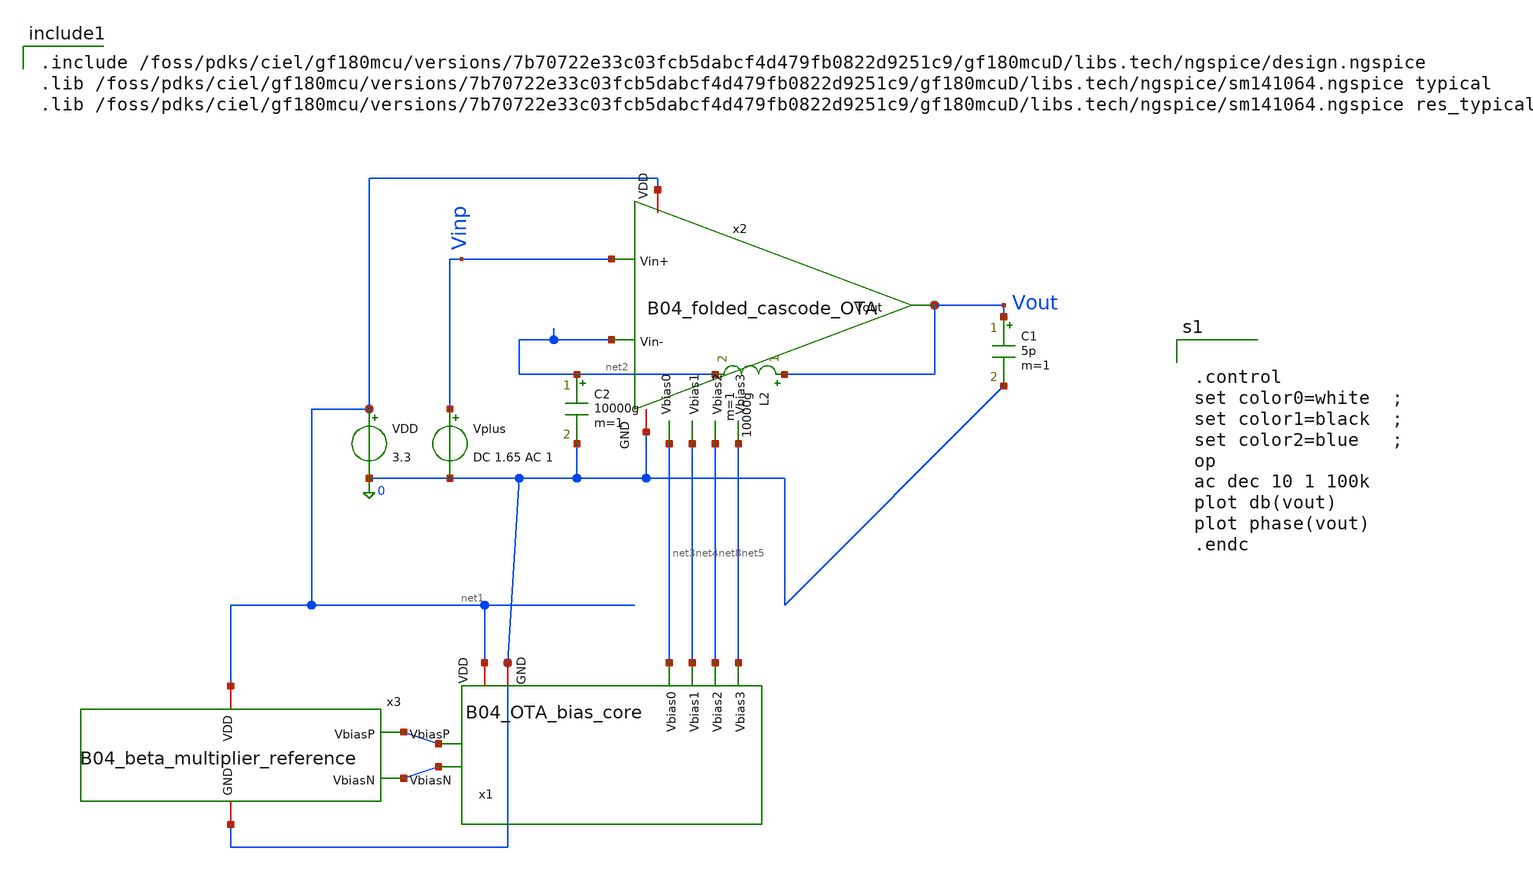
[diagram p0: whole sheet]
** sch_path: analog/B04_tb_OTA.sch
**.subckt B04_tb_OTA
VDD net1 0 3.3
Vplus Vinp 0 DC 1.65 AC 1
x1 net1 net6 net3 net8 net5 net4 net7 0 B04_OTA_bias_core ratio=0.25
x3 net1 net6 net7 0 B04_beta_multiplier_reference length=410u
C1 Vout 0 5p m=1
C2 net2 0 10000g m=1
L2 Vout net2 10000g m=1
x2 net1 net3 Vinp net2 net5 net4 Vout net8 0 B04_folded_cascode_OTA
**** begin user architecture code


.control
set color0=white  ;
set color1=black  ;
set color2=blue   ;
op
ac dec 10 1 100k
plot db(vout)
plot phase(vout)
.endc



.include /foss/pdks/ciel/gf180mcu/versions/7b70722e33c03fcb5dabcf4d479fb0822d9251c9/gf180mcuD/libs.tech/ngspice/design.ngspice
.lib /foss/pdks/ciel/gf180mcu/versions/7b70722e33c03fcb5dabcf4d479fb0822d9251c9/gf180mcuD/libs.tech/ngspice/sm141064.ngspice typical
.lib /foss/pdks/ciel/gf180mcu/versions/7b70722e33c03fcb5dabcf4d479fb0822d9251c9/gf180mcuD/libs.tech/ngspice/sm141064.ngspice res_typical

**** end user architecture code
**.ends

* expanding   symbol:
*+  AURA-Event-Driven-Mixed-Signal-ASIC-for-Acoustic-Pattern-Detection/analog/B04_OTA_bias_core.sym # of pins=8
** sym_path: analog/B04_OTA_bias_core.sym
** sch_path: analog/B04_OTA_bias_core.sch
.subckt B04_OTA_bias_core VDD VbiasP Vbias0 Vbias2 Vbias3 Vbias1 VbiasN GND  ratio=1
*.iopin VDD
*.opin Vbias2
*.opin Vbias1
*.opin Vbias0
*.opin Vbias3
*.iopin GND
*.ipin VbiasP
*.ipin VbiasN
XM1 Vbias1 GND Vbias2 VDD pfet_03v3 L=4u W=5u nf=1 ad='int((nf+1)/2) * W/nf * 0.18u' as='int((nf+2)/2) * W/nf * 0.18u'
+ pd='2*int((nf+1)/2) * (W/nf + 0.18u)' ps='2*int((nf+2)/2) * (W/nf + 0.18u)' nrd='0.18u / W' nrs='0.18u / W'
+ sa=0 sb=0 sd=0 m=1
XM4 Vbias1 Vbias2 net1 GND nfet_03v3 L=4u W=1u nf=1 ad='int((nf+1)/2) * W/nf * 0.18u' as='int((nf+2)/2) * W/nf * 0.18u'
+ pd='2*int((nf+1)/2) * (W/nf + 0.18u)' ps='2*int((nf+2)/2) * (W/nf + 0.18u)' nrd='0.18u / W' nrs='0.18u / W'
+ sa=0 sb=0 sd=0 m=1
XM5 net1 Vbias1 GND GND nfet_03v3 L=4u W=1u nf=1 ad='int((nf+1)/2) * W/nf * 0.18u' as='int((nf+2)/2) * W/nf * 0.18u'
+ pd='2*int((nf+1)/2) * (W/nf + 0.18u)' ps='2*int((nf+2)/2) * (W/nf + 0.18u)' nrd='0.18u / W' nrs='0.18u / W'
+ sa=0 sb=0 sd=0 m=1
XM9 net2 Vbias3 Vbias0 VDD pfet_03v3 L=4u W=5u nf=1 ad='int((nf+1)/2) * W/nf * 0.18u' as='int((nf+2)/2) * W/nf * 0.18u'
+ pd='2*int((nf+1)/2) * (W/nf + 0.18u)' ps='2*int((nf+2)/2) * (W/nf + 0.18u)' nrd='0.18u / W' nrs='0.18u / W'
+ sa=0 sb=0 sd=0 m=1
XM10 VDD Vbias0 net2 VDD pfet_03v3 L=4u W=5u nf=1 ad='int((nf+1)/2) * W/nf * 0.18u' as='int((nf+2)/2) * W/nf * 0.18u'
+ pd='2*int((nf+1)/2) * (W/nf + 0.18u)' ps='2*int((nf+2)/2) * (W/nf + 0.18u)' nrd='0.18u / W' nrs='0.18u / W'
+ sa=0 sb=0 sd=0 m=1
XM6 Vbias3 VDD Vbias0 GND nfet_03v3 L=4u W=10u nf=1 ad='int((nf+1)/2) * W/nf * 0.18u' as='int((nf+2)/2) * W/nf * 0.18u'
+ pd='2*int((nf+1)/2) * (W/nf + 0.18u)' ps='2*int((nf+2)/2) * (W/nf + 0.18u)' nrd='0.18u / W' nrs='0.18u / W'
+ sa=0 sb=0 sd=0 m=1
XM2 Vbias2 VbiasP VDD VDD pfet_03v3 L=4u W={ratio*5u} nf=1 ad='int((nf+1)/2) * W/nf * 0.18u' as='int((nf+2)/2) * W/nf * 0.18u'
+ pd='2*int((nf+1)/2) * (W/nf + 0.18u)' ps='2*int((nf+2)/2) * (W/nf + 0.18u)' nrd='0.18u / W' nrs='0.18u / W'
+ sa=0 sb=0 sd=0 m=1
XM3 GND VbiasN Vbias3 GND nfet_03v3 L=4u W={ratio*10u} nf=1 ad='int((nf+1)/2) * W/nf * 0.18u' as='int((nf+2)/2) * W/nf * 0.18u'
+ pd='2*int((nf+1)/2) * (W/nf + 0.18u)' ps='2*int((nf+2)/2) * (W/nf + 0.18u)' nrd='0.18u / W' nrs='0.18u / W'
+ sa=0 sb=0 sd=0 m=1
.ends


* expanding   symbol:
*+  AURA-Event-Driven-Mixed-Signal-ASIC-for-Acoustic-Pattern-Detection/analog/B04_beta_multiplier_reference.sym # of pins=4
** sym_path: analog/B04_beta_multiplier_reference.sym
** sch_path: analog/B04_beta_multiplier_reference.sch
.subckt B04_beta_multiplier_reference VDD VbiasP VbiasN GND  length=410u
*.iopin VDD
*.iopin GND
*.opin VbiasP
*.opin VbiasN
XM2 VbiasN VbiasP VDD VDD pfet_03v3 L=4u W=2u nf=1 ad='int((nf+1)/2) * W/nf * 0.18u' as='int((nf+2)/2) * W/nf * 0.18u'
+ pd='2*int((nf+1)/2) * (W/nf + 0.18u)' ps='2*int((nf+2)/2) * (W/nf + 0.18u)' nrd='0.18u / W' nrs='0.18u / W'
+ sa=0 sb=0 sd=0 m=1
XM3 net2 VbiasP VDD VDD pfet_03v3 L=4u W=2u nf=1 ad='int((nf+1)/2) * W/nf * 0.18u' as='int((nf+2)/2) * W/nf * 0.18u'
+ pd='2*int((nf+1)/2) * (W/nf + 0.18u)' ps='2*int((nf+2)/2) * (W/nf + 0.18u)' nrd='0.18u / W' nrs='0.18u / W'
+ sa=0 sb=0 sd=0 m=1
XM6 VbiasN VbiasN GND GND nfet_03v3 L=4u W=10u nf=1 ad='int((nf+1)/2) * W/nf * 0.18u' as='int((nf+2)/2) * W/nf * 0.18u'
+ pd='2*int((nf+1)/2) * (W/nf + 0.18u)' ps='2*int((nf+2)/2) * (W/nf + 0.18u)' nrd='0.18u / W' nrs='0.18u / W'
+ sa=0 sb=0 sd=0 m=1
XM7 net2 VbiasN net1 GND nfet_03v3 L=4u W=10u nf=1 ad='int((nf+1)/2) * W/nf * 0.18u' as='int((nf+2)/2) * W/nf * 0.18u'
+ pd='2*int((nf+1)/2) * (W/nf + 0.18u)' ps='2*int((nf+2)/2) * (W/nf + 0.18u)' nrd='0.18u / W' nrs='0.18u / W'
+ sa=0 sb=0 sd=0 m=4
XM1 net4 net4 VDD VDD pfet_03v3 L=40u W=0.22u nf=1 ad='int((nf+1)/2) * W/nf * 0.18u' as='int((nf+2)/2) * W/nf * 0.18u'
+ pd='2*int((nf+1)/2) * (W/nf + 0.18u)' ps='2*int((nf+2)/2) * (W/nf + 0.18u)' nrd='0.18u / W' nrs='0.18u / W'
+ sa=0 sb=0 sd=0 m=1
XM4 VbiasP net3 VbiasN GND nfet_03v3 L=1u W=1u nf=1 ad='int((nf+1)/2) * W/nf * 0.18u' as='int((nf+2)/2) * W/nf * 0.18u'
+ pd='2*int((nf+1)/2) * (W/nf + 0.18u)' ps='2*int((nf+2)/2) * (W/nf + 0.18u)' nrd='0.18u / W' nrs='0.18u / W'
+ sa=0 sb=0 sd=0 m=1
XM5 net3 VbiasN GND GND nfet_03v3 L=10u W=1u nf=1 ad='int((nf+1)/2) * W/nf * 0.18u' as='int((nf+2)/2) * W/nf * 0.18u'
+ pd='2*int((nf+1)/2) * (W/nf + 0.18u)' ps='2*int((nf+2)/2) * (W/nf + 0.18u)' nrd='0.18u / W' nrs='0.18u / W'
+ sa=0 sb=0 sd=0 m=1
XM8 net5 net5 net4 VDD pfet_03v3 L=40u W=0.22u nf=1 ad='int((nf+1)/2) * W/nf * 0.18u' as='int((nf+2)/2) * W/nf * 0.18u'
+ pd='2*int((nf+1)/2) * (W/nf + 0.18u)' ps='2*int((nf+2)/2) * (W/nf + 0.18u)' nrd='0.18u / W' nrs='0.18u / W'
+ sa=0 sb=0 sd=0 m=1
XM9 net3 net5 net5 VDD pfet_03v3 L=40u W=0.22u nf=1 ad='int((nf+1)/2) * W/nf * 0.18u' as='int((nf+2)/2) * W/nf * 0.18u'
+ pd='2*int((nf+1)/2) * (W/nf + 0.18u)' ps='2*int((nf+2)/2) * (W/nf + 0.18u)' nrd='0.18u / W' nrs='0.18u / W'
+ sa=0 sb=0 sd=0 m=1
XR2 GND net1 GND ppolyf_u_2k r_width=2u r_length={length} m=1
x1 VDD VbiasP net2 VbiasN VbiasN GND B04_diff_amp
.ends


* expanding   symbol:
*+  AURA-Event-Driven-Mixed-Signal-ASIC-for-Acoustic-Pattern-Detection/analog/B04_folded_cascode_OTA.sym # of pins=9
** sym_path: analog/B04_folded_cascode_OTA.sym
** sch_path: analog/B04_folded_cascode_OTA.sch
.subckt B04_folded_cascode_OTA VDD Vbias0 Vin+ Vin- Vbias3 Vbias1 Vout Vbias2 GND
*.iopin VDD
*.ipin Vbias0
*.ipin Vin+
*.ipin Vin-
*.opin Vout
*.ipin Vbias3
*.ipin Vbias2
*.iopin GND
*.ipin Vbias1
XM1 net1 Vbias0 VDD VDD pfet_03v3 L=4u W=5u nf=2 ad='int((nf+1)/2) * W/nf * 0.18u' as='int((nf+2)/2) * W/nf * 0.18u'
+ pd='2*int((nf+1)/2) * (W/nf + 0.18u)' ps='2*int((nf+2)/2) * (W/nf + 0.18u)' nrd='0.18u / W' nrs='0.18u / W'
+ sa=0 sb=0 sd=0 m=1
XM2 net6 Vin+ net1 VDD pfet_03v3 L=1u W=2u nf=9 ad='int((nf+1)/2) * W/nf * 0.18u' as='int((nf+2)/2) * W/nf * 0.18u'
+ pd='2*int((nf+1)/2) * (W/nf + 0.18u)' ps='2*int((nf+2)/2) * (W/nf + 0.18u)' nrd='0.18u / W' nrs='0.18u / W'
+ sa=0 sb=0 sd=0 m=1
XM3 net7 Vin- net1 VDD pfet_03v3 L=1u W=2u nf=9 ad='int((nf+1)/2) * W/nf * 0.18u' as='int((nf+2)/2) * W/nf * 0.18u'
+ pd='2*int((nf+1)/2) * (W/nf + 0.18u)' ps='2*int((nf+2)/2) * (W/nf + 0.18u)' nrd='0.18u / W' nrs='0.18u / W'
+ sa=0 sb=0 sd=0 m=1
XM4 net2 Vin+ net1 VDD pfet_03v3 L=1u W=2u nf=1 ad='int((nf+1)/2) * W/nf * 0.18u' as='int((nf+2)/2) * W/nf * 0.18u'
+ pd='2*int((nf+1)/2) * (W/nf + 0.18u)' ps='2*int((nf+2)/2) * (W/nf + 0.18u)' nrd='0.18u / W' nrs='0.18u / W'
+ sa=0 sb=0 sd=0 m=1
XM5 net3 Vin- net1 VDD pfet_03v3 L=1u W=2u nf=1 ad='int((nf+1)/2) * W/nf * 0.18u' as='int((nf+2)/2) * W/nf * 0.18u'
+ pd='2*int((nf+1)/2) * (W/nf + 0.18u)' ps='2*int((nf+2)/2) * (W/nf + 0.18u)' nrd='0.18u / W' nrs='0.18u / W'
+ sa=0 sb=0 sd=0 m=1
XM6 net2 Vbias2 net5 0 nfet_03v3 L=1u W=2u nf=1 ad='int((nf+1)/2) * W/nf * 0.18u' as='int((nf+2)/2) * W/nf * 0.18u'
+ pd='2*int((nf+1)/2) * (W/nf + 0.18u)' ps='2*int((nf+2)/2) * (W/nf + 0.18u)' nrd='0.18u / W' nrs='0.18u / W'
+ sa=0 sb=0 sd=0 m=1
XM7 net3 Vbias2 net4 0 nfet_03v3 L=1u W=2u nf=1 ad='int((nf+1)/2) * W/nf * 0.18u' as='int((nf+2)/2) * W/nf * 0.18u'
+ pd='2*int((nf+1)/2) * (W/nf + 0.18u)' ps='2*int((nf+2)/2) * (W/nf + 0.18u)' nrd='0.18u / W' nrs='0.18u / W'
+ sa=0 sb=0 sd=0 m=1
XM8 net5 net2 GND GND nfet_03v3 L=4u W=1u nf=1 ad='int((nf+1)/2) * W/nf * 0.18u' as='int((nf+2)/2) * W/nf * 0.18u'
+ pd='2*int((nf+1)/2) * (W/nf + 0.18u)' ps='2*int((nf+2)/2) * (W/nf + 0.18u)' nrd='0.18u / W' nrs='0.18u / W'
+ sa=0 sb=0 sd=0 m=1
XM9 net6 net3 GND GND nfet_03v3 L=4u W=1u nf=1 ad='int((nf+1)/2) * W/nf * 0.18u' as='int((nf+2)/2) * W/nf * 0.18u'
+ pd='2*int((nf+1)/2) * (W/nf + 0.18u)' ps='2*int((nf+2)/2) * (W/nf + 0.18u)' nrd='0.18u / W' nrs='0.18u / W'
+ sa=0 sb=0 sd=0 m=1
XM10 net4 net3 GND GND nfet_03v3 L=4u W=1u nf=1 ad='int((nf+1)/2) * W/nf * 0.18u' as='int((nf+2)/2) * W/nf * 0.18u'
+ pd='2*int((nf+1)/2) * (W/nf + 0.18u)' ps='2*int((nf+2)/2) * (W/nf + 0.18u)' nrd='0.18u / W' nrs='0.18u / W'
+ sa=0 sb=0 sd=0 m=1
XM11 net7 net2 GND GND nfet_03v3 L=4u W=1u nf=1 ad='int((nf+1)/2) * W/nf * 0.18u' as='int((nf+2)/2) * W/nf * 0.18u'
+ pd='2*int((nf+1)/2) * (W/nf + 0.18u)' ps='2*int((nf+2)/2) * (W/nf + 0.18u)' nrd='0.18u / W' nrs='0.18u / W'
+ sa=0 sb=0 sd=0 m=1
XM12 net9 net10 VDD VDD pfet_03v3 L=4u W=5u nf=1 ad='int((nf+1)/2) * W/nf * 0.18u' as='int((nf+2)/2) * W/nf * 0.18u'
+ pd='2*int((nf+1)/2) * (W/nf + 0.18u)' ps='2*int((nf+2)/2) * (W/nf + 0.18u)' nrd='0.18u / W' nrs='0.18u / W'
+ sa=0 sb=0 sd=0 m=1
XM13 net8 net10 VDD VDD pfet_03v3 L=4u W=5u nf=1 ad='int((nf+1)/2) * W/nf * 0.18u' as='int((nf+2)/2) * W/nf * 0.18u'
+ pd='2*int((nf+1)/2) * (W/nf + 0.18u)' ps='2*int((nf+2)/2) * (W/nf + 0.18u)' nrd='0.18u / W' nrs='0.18u / W'
+ sa=0 sb=0 sd=0 m=1
XM14 Vout Vbias3 net9 VDD pfet_03v3 L=4u W=5u nf=1 ad='int((nf+1)/2) * W/nf * 0.18u' as='int((nf+2)/2) * W/nf * 0.18u'
+ pd='2*int((nf+1)/2) * (W/nf + 0.18u)' ps='2*int((nf+2)/2) * (W/nf + 0.18u)' nrd='0.18u / W' nrs='0.18u / W'
+ sa=0 sb=0 sd=0 m=1
XM15 net10 Vbias3 net8 VDD pfet_03v3 L=4u W=5u nf=1 ad='int((nf+1)/2) * W/nf * 0.18u' as='int((nf+2)/2) * W/nf * 0.18u'
+ pd='2*int((nf+1)/2) * (W/nf + 0.18u)' ps='2*int((nf+2)/2) * (W/nf + 0.18u)' nrd='0.18u / W' nrs='0.18u / W'
+ sa=0 sb=0 sd=0 m=1
XM16 Vout Vbias2 net7 0 nfet_03v3 L=4u W=1u nf=1 ad='int((nf+1)/2) * W/nf * 0.18u' as='int((nf+2)/2) * W/nf * 0.18u'
+ pd='2*int((nf+1)/2) * (W/nf + 0.18u)' ps='2*int((nf+2)/2) * (W/nf + 0.18u)' nrd='0.18u / W' nrs='0.18u / W'
+ sa=0 sb=0 sd=0 m=1
XM17 net10 Vbias2 net6 0 nfet_03v3 L=4u W=1u nf=1 ad='int((nf+1)/2) * W/nf * 0.18u' as='int((nf+2)/2) * W/nf * 0.18u'
+ pd='2*int((nf+1)/2) * (W/nf + 0.18u)' ps='2*int((nf+2)/2) * (W/nf + 0.18u)' nrd='0.18u / W' nrs='0.18u / W'
+ sa=0 sb=0 sd=0 m=1
XM18 net6 Vbias1 GND GND nfet_03v3 L=4u W=1u nf=10 ad='int((nf+1)/2) * W/nf * 0.18u' as='int((nf+2)/2) * W/nf * 0.18u'
+ pd='2*int((nf+1)/2) * (W/nf + 0.18u)' ps='2*int((nf+2)/2) * (W/nf + 0.18u)' nrd='0.18u / W' nrs='0.18u / W'
+ sa=0 sb=0 sd=0 m=1
XM19 net7 Vbias1 GND GND nfet_03v3 L=4u W=1u nf=10 ad='int((nf+1)/2) * W/nf * 0.18u' as='int((nf+2)/2) * W/nf * 0.18u'
+ pd='2*int((nf+1)/2) * (W/nf + 0.18u)' ps='2*int((nf+2)/2) * (W/nf + 0.18u)' nrd='0.18u / W' nrs='0.18u / W'
+ sa=0 sb=0 sd=0 m=1
.ends


* expanding   symbol:
*+  AURA-Event-Driven-Mixed-Signal-ASIC-for-Acoustic-Pattern-Detection/analog/B04_diff_amp.sym # of pins=6
** sym_path: analog/B04_diff_amp.sym
** sch_path: analog/B04_diff_amp.sch
.subckt B04_diff_amp VDD Vo V+ V- Vbias VSS
*.iopin VDD
*.iopin VSS
*.ipin V+
*.ipin V-
*.opin Vo
*.ipin Vbias
XM1 net1 V+ net2 VSS nfet_03v3 L=4u W=1.1u nf=1 ad='int((nf+1)/2) * W/nf * 0.18u' as='int((nf+2)/2) * W/nf * 0.18u'
+ pd='2*int((nf+1)/2) * (W/nf + 0.18u)' ps='2*int((nf+2)/2) * (W/nf + 0.18u)' nrd='0.18u / W' nrs='0.18u / W'
+ sa=0 sb=0 sd=0 m=1
XM2 net2 Vbias VSS VSS nfet_03v3 L=4u W=2.2u nf=1 ad='int((nf+1)/2) * W/nf * 0.18u' as='int((nf+2)/2) * W/nf * 0.18u'
+ pd='2*int((nf+1)/2) * (W/nf + 0.18u)' ps='2*int((nf+2)/2) * (W/nf + 0.18u)' nrd='0.18u / W' nrs='0.18u / W'
+ sa=0 sb=0 sd=0 m=1
XM3 Vo V- net2 VSS nfet_03v3 L=4u W=1.1u nf=1 ad='int((nf+1)/2) * W/nf * 0.18u' as='int((nf+2)/2) * W/nf * 0.18u'
+ pd='2*int((nf+1)/2) * (W/nf + 0.18u)' ps='2*int((nf+2)/2) * (W/nf + 0.18u)' nrd='0.18u / W' nrs='0.18u / W'
+ sa=0 sb=0 sd=0 m=1
XM4 Vo net1 VDD VDD pfet_03v3 L=4u W=13u nf=1 ad='int((nf+1)/2) * W/nf * 0.18u' as='int((nf+2)/2) * W/nf * 0.18u'
+ pd='2*int((nf+1)/2) * (W/nf + 0.18u)' ps='2*int((nf+2)/2) * (W/nf + 0.18u)' nrd='0.18u / W' nrs='0.18u / W'
+ sa=0 sb=0 sd=0 m=1
XM5 net1 net1 VDD VDD pfet_03v3 L=4u W=13u nf=1 ad='int((nf+1)/2) * W/nf * 0.18u' as='int((nf+2)/2) * W/nf * 0.18u'
+ pd='2*int((nf+1)/2) * (W/nf + 0.18u)' ps='2*int((nf+2)/2) * (W/nf + 0.18u)' nrd='0.18u / W' nrs='0.18u / W'
+ sa=0 sb=0 sd=0 m=1
XMDummy VDD VDD VDD VDD pfet_03v3 L=4u W=6.5u nf=1 ad='int((nf+1)/2) * W/nf * 0.18u' as='int((nf+2)/2) * W/nf * 0.18u'
+ pd='2*int((nf+1)/2) * (W/nf + 0.18u)' ps='2*int((nf+2)/2) * (W/nf + 0.18u)' nrd='0.18u / W' nrs='0.18u / W'
+ sa=0 sb=0 sd=0 m=1
XMDummy1 VDD VDD VDD VDD pfet_03v3 L=4u W=6.5u nf=1 ad='int((nf+1)/2) * W/nf * 0.18u' as='int((nf+2)/2) * W/nf * 0.18u'
+ pd='2*int((nf+1)/2) * (W/nf + 0.18u)' ps='2*int((nf+2)/2) * (W/nf + 0.18u)' nrd='0.18u / W' nrs='0.18u / W'
+ sa=0 sb=0 sd=0 m=1
XMdummy2 VSS VSS VSS VSS nfet_03v3 L=4u W=0.55u nf=1 ad='int((nf+1)/2) * W/nf * 0.18u' as='int((nf+2)/2) * W/nf * 0.18u'
+ pd='2*int((nf+1)/2) * (W/nf + 0.18u)' ps='2*int((nf+2)/2) * (W/nf + 0.18u)' nrd='0.18u / W' nrs='0.18u / W'
+ sa=0 sb=0 sd=0 m=1
XMdummy3 VSS VSS VSS VSS nfet_03v3 L=4u W=0.55u nf=1 ad='int((nf+1)/2) * W/nf * 0.18u' as='int((nf+2)/2) * W/nf * 0.18u'
+ pd='2*int((nf+1)/2) * (W/nf + 0.18u)' ps='2*int((nf+2)/2) * (W/nf + 0.18u)' nrd='0.18u / W' nrs='0.18u / W'
+ sa=0 sb=0 sd=0 m=1
.ends

.end
